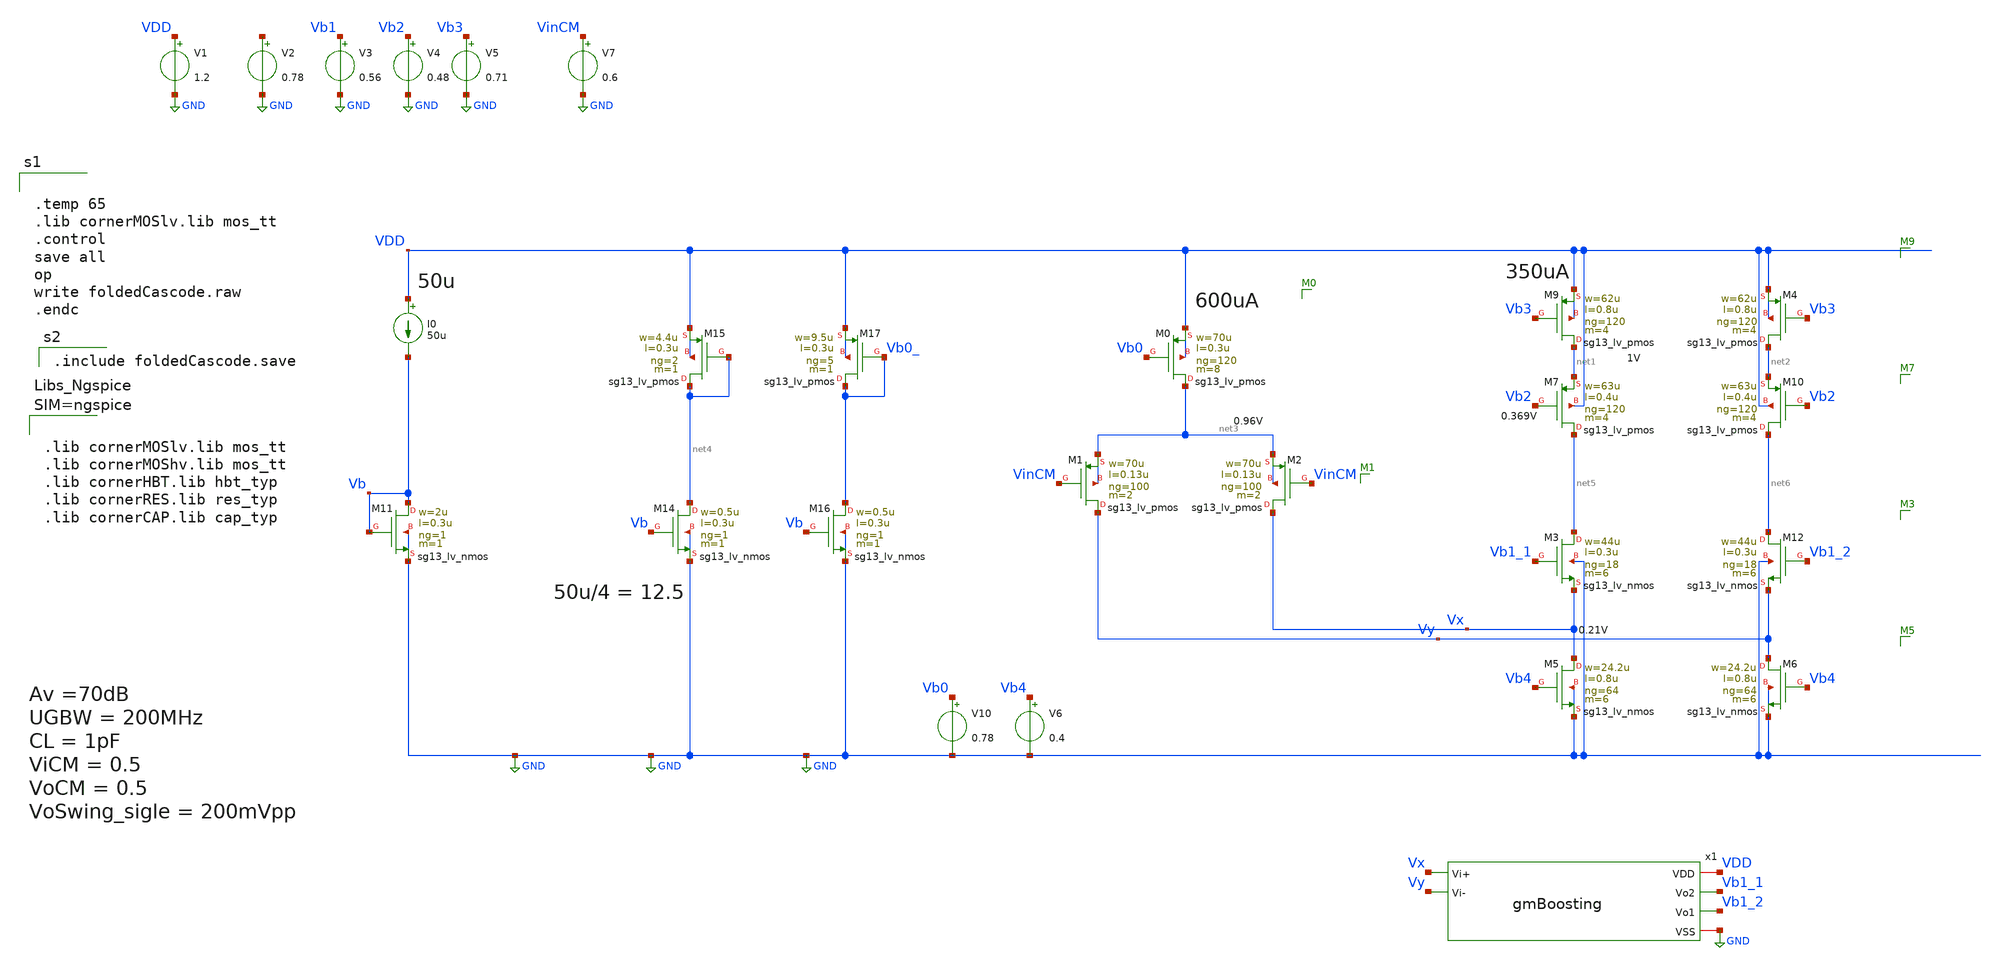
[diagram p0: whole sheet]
** sch_path: sch/testing/foldedCascode.sch
**.subckt foldedCascode
V1 VDD GND 1.2
XM5 Vx Vb4 GND GND sg13_lv_nmos w=24.2u l=0.8u ng=64 m=6 mm_ok=1
XM6 Vy Vb4 GND GND sg13_lv_nmos w=24.2u l=0.8u ng=64 m=6 mm_ok=1
XM9 net1 Vb3 VDD VDD sg13_lv_pmos w=62u l=0.8u ng=120 m=4 mm_ok=1
V2 net7 GND 0.78
V3 Vb1 GND 0.56
V4 Vb2 GND 0.48
V5 Vb3 GND 0.71
V7 VinCM GND 0.6
XM1 Vy VinCM net3 net3 sg13_lv_pmos w=70u l=0.13u ng=100 m=2 mm_ok=1
XM0 net3 Vb0 VDD VDD sg13_lv_pmos w=70u l=0.3u ng=120 m=8 mm_ok=1
I0 VDD Vb 50u
XM11 Vb Vb GND GND sg13_lv_nmos w=2u l=0.3u ng=1 m=1 mm_ok=1
XM14 net4 Vb GND GND sg13_lv_nmos w=0.5u l=0.3u ng=1 m=1 mm_ok=1
XM15 net4 net4 VDD VDD sg13_lv_pmos w=4.4u l=0.3u ng=2 m=1 mm_ok=1
XM16 Vb0_ Vb GND GND sg13_lv_nmos w=0.5u l=0.3u ng=1 m=1 mm_ok=1
XM17 Vb0_ Vb0_ VDD VDD sg13_lv_pmos w=9.5u l=0.3u ng=5 m=1 mm_ok=1
x1 VDD Vb1_1 Vb1_2 Vx Vy GND gmBoosting
XM7 net5 Vb2 net1 VDD sg13_lv_pmos w=63u l=0.4u ng=120 m=4 mm_ok=1
XM2 Vx VinCM net3 net3 sg13_lv_pmos w=70u l=0.13u ng=100 m=2 mm_ok=1
V10 Vb0 GND 0.78
XM4 net2 Vb3 VDD VDD sg13_lv_pmos w=62u l=0.8u ng=120 m=4 mm_ok=1
XM10 net6 Vb2 net2 VDD sg13_lv_pmos w=63u l=0.4u ng=120 m=4 mm_ok=1
V6 Vb4 GND 0.4
XM3 net5 Vb1_1 Vx GND sg13_lv_nmos w=44u l=0.3u ng=18 m=6 mm_ok=1
XM12 net6 Vb1_2 Vy GND sg13_lv_nmos w=44u l=0.3u ng=18 m=6 mm_ok=1
**** begin user architecture code


.temp 65
.lib cornerMOSlv.lib mos_tt
.control
save all
op
write foldedCascode.raw
.endc



.include foldedCascode.save




.lib cornerMOSlv.lib mos_tt
.lib cornerMOShv.lib mos_tt
.lib cornerHBT.lib hbt_typ
.lib cornerRES.lib res_typ
.lib cornerCAP.lib cap_typ



**** end user architecture code
**.ends

* expanding   symbol:  gmBoosting.sym # of pins=6
** sym_path: sch/blocks/gmBoosting.sym
** sch_path: sch/blocks/gmBoosting.sch
.subckt gmBoosting VDD Vo2 Vo1 Vi+ Vi- VSS
*.iopin VSS
*.opin Vo1
*.opin Vo2
*.ipin Vi+
*.ipin Vi-
*.iopin VDD
V1 Vref VSS 0.55
XM7 net2 Vb4 VDD VDD sg13_lv_pmos w=25u l=0.7u ng=13 m=2 mm_ok=1
XM1 net8 Vi+ net1 net1 sg13_lv_pmos w=40u l=0.15u ng=80 m=4 mm_ok=1
XM2 net4 Vi- net1 net1 sg13_lv_pmos w=40u l=0.15u ng=80 m=4 mm_ok=1
XM0 net1 Vb0 net5 VDD sg13_lv_pmos w=16u l=0.3u ng=20 m=1 mm_ok=1
XM6 net8 Vb3 VSS VSS sg13_lv_nmos w=20u l=0.7u ng=5 m=2 mm_ok=1
XM9 Vo1 Vb2 net2 VDD sg13_lv_pmos w=30u l=0.3u ng=10 m=1 mm_ok=1
XM10 Vo2 Vb2 net3 VDD sg13_lv_pmos w=30u l=0.3u ng=10 m=1 mm_ok=1
XM8 net3 Vb4 VDD VDD sg13_lv_pmos w=25u l=0.7u ng=13 m=2 mm_ok=1
XM3 net5 Vo2 VDD VDD sg13_lv_pmos w=20u l=0.13u ng=5 m=1 mm_ok=1
XM4 net5 Vo1 VDD VDD sg13_lv_pmos w=20u l=0.13u ng=5 m=1 mm_ok=1
XM5 net6 Vref VDD VDD sg13_lv_pmos w=20u l=0.13u ng=5 m=2 mm_ok=1
XM28 Vb0 net7 VSS VSS sg13_lv_nmos w=10u l=0.2u ng=2 m=1 mm_ok=1
XM29 Vb3 Vb3 VSS VSS sg13_lv_nmos w=30u l=0.2u ng=4 m=1 mm_ok=1
XR16 net7 Vb0 sub! rppd w=0.8e-6 l=2.5e-6 m=1 b=0 mm_ok=1
XM30 Vb3 Vb0 net6 VDD sg13_lv_pmos w=16u l=0.3u ng=20 m=1 mm_ok=1
XM31 net4 Vb3 VSS VSS sg13_lv_nmos w=20u l=0.7u ng=5 m=2 mm_ok=1
XM32 Vo1 Vb1 net4 VSS sg13_lv_nmos w=37.5u l=0.7u ng=5 m=1 mm_ok=1
XM33 Vo2 Vb1 net8 VSS sg13_lv_nmos w=37.5u l=0.7u ng=5 m=1 mm_ok=1
XM23 net7 Vbb VDD VDD sg13_lv_pmos w=18u l=1u ng=18 m=1 mm_ok=1
XR9 Vb1 net10 sub! rhigh w=0.5e-6 l=2.31e-6 m=1 b=0 mm_ok=1
XM17 net10 Vb1 net9 VSS sg13_lv_nmos w=25u l=0.7u ng=3 m=1 mm_ok=1
XM18 net9 net10 VSS VSS sg13_lv_nmos w=40u l=0.7u ng=4 m=1 mm_ok=1
XM19 net11 Vb4 VDD VDD sg13_lv_pmos w=15u l=0.7u ng=5 m=1 mm_ok=1
XM20 Vb4 Vb2 net11 VDD sg13_lv_pmos w=7u l=0.3u ng=7 m=1 mm_ok=1
XR10 Vb4 Vb2 sub! rhigh w=0.5e-6 l=1.8e-6 m=1 b=0 mm_ok=1
I3 Vbb VSS 50u
XM21 Vbb Vbb VDD VDD sg13_lv_pmos w=18u l=1u ng=18 m=1 mm_ok=1
XM22 Vb1 Vbb VDD VDD sg13_lv_pmos w=18u l=1u ng=18 m=1 mm_ok=1
XM24 net12 Vbb VDD VDD sg13_lv_pmos w=18u l=1u ng=18 m=1 mm_ok=1
XM25 net12 net12 VSS VSS sg13_lv_nmos w=15u l=1u ng=2 m=1 mm_ok=1
XM26 Vb2 net12 VSS VSS sg13_lv_nmos w=15u l=1u ng=2 m=1 mm_ok=1
.ends

.GLOBAL GND
.end
